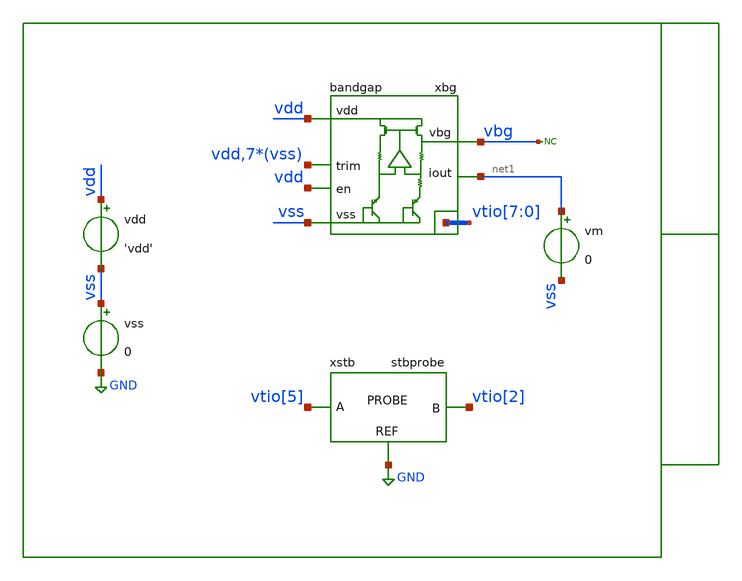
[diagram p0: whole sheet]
** sch_path: xschem/tb/bandgap_cm/bandgap/ac_bandgap_stb.sch
**.subckt ac_bandgap_stb
xbg vdd vbg vss vtio[7] vtio[6] vtio[5] vtio[4] vtio[3] vtio[2] vtio[1] vtio[0] vdd vss vss vss vss
+ vss vss vss net1 vdd bandgap
vdd vdd vss 'vdd'
vss vss GND 0
* noconn vbg
vm net1 vss 0
xstb vtio[5] vtio[2] GND stbprobe
**** begin user architecture code

* Control

.param vdd = 3.3

.temp 27

.options reltol  = 1e-6
.options abstol  = 1e-12
.options gmin    = 1e-15

*------------------------------------------------------------
* Nodeset for better convergence
*------------------------------------------------------------
.nodeset v(vbg)  = '1'
.nodeset v(xbg.gate) = 'vdd/2'
.nodeset v(xbg.vx)   = '0.70'
.nodeset v(xbg.vbe2) = '0.65'
.nodeset v(xbg.vs1)  = '0'
*------------------------------------------------------------


.control

let runs=2
let run=0

alter v.xstb.vprobe1 acmag=1
alter i.xstb.iprobe1 acmag=0

dowhile run < runs
set run ="$&run"

ac dec 100 0.01 10G

alter v.xstb.vprobe1 acmag=0
alter i.xstb.iprobe1 acmag=1

let run = run + 1

end

let ip11 = ac1.i(v.xstb.vprobe1)
let ip12 = ac1.i(v.xstb.vprobe2)
let ip21 = ac2.i(v.xstb.vprobe1)
let ip22 = ac2.i(v.xstb.vprobe2)
let vprb1 = ac1.v(xstb.probe)
let vprb2 = ac2.v(xstb.probe)

let av = 1/(1/(2*(ip11*vprb2-vprb1*ip21)+vprb1+ip21)-1)

let phase=180/PI*cph(av)

gnuplot p1 vdb(av)
gnuplot p2 phase

meas ac gain find vdb(av) at=0.01
meas ac ugbw when vdb(av)=0
meas ac pm_pha find phase when vdb(av)=0

let pm = 180 + pm_pha
print gain
print ugbw
print pm

set wr_singlescale
set wr_vecnames
wrdata data.csv vdb(av) phase

.endc
.end


 * Model Corners

.include $::CORNERS/ngspice/tt.spice
*.include $::CORNERS/ngspice/ff.spice
*.include $::CORNERS/ngspice/ss.spice
*.include $::CORNERS/ngspice/sf.spice
*.include $::CORNERS/ngspice/fs.spice

**** end user architecture code
**.ends
.GLOBAL GND
.end
